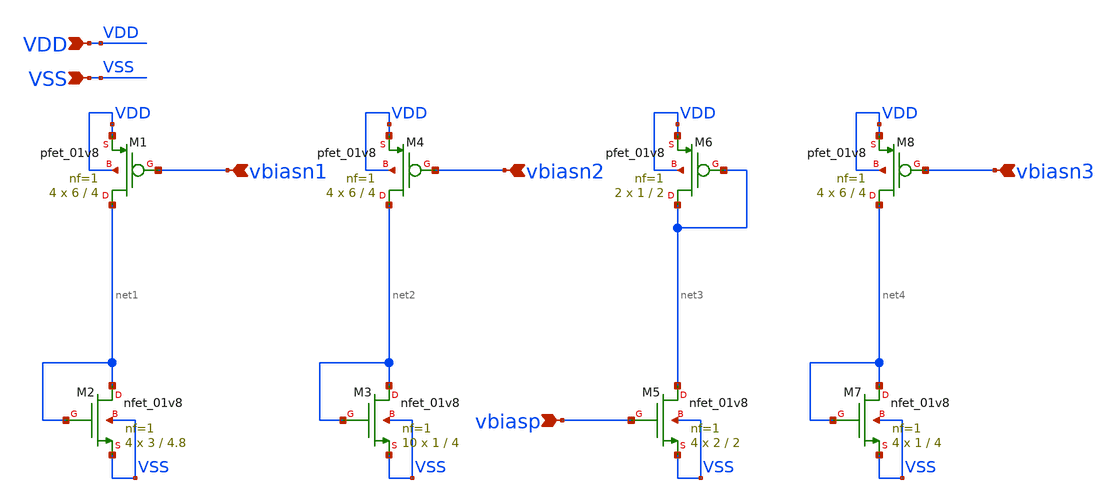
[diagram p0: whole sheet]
** sch_path: designs/bias_current_distribution.sch
* Copyright 2020 Stefan Frederik Schippers
* Licensed under the Apache License, Version 2.0 (the "License");
* you may not use this file except in compliance with the License.
* You may obtain a copy of the License at
* https://www.apache.org/licenses/LICENSE-2.0
* Unless required by applicable law or agreed to in writing, software
* distributed under the License is distributed on an "AS IS" BASIS,
* WITHOUT WARRANTIES OR CONDITIONS OF ANY KIND, either express or implied.
* See the License for the specific language governing permissions and
* limitations under the License.
**.subckt bias_current_distribution VDD VSS vbiasn1 vbiasn2 vbiasp vbiasn3
*.ipin VDD
*.ipin VSS
*.ipin vbiasn1
*.ipin vbiasn2
*.ipin vbiasp
*.ipin vbiasn3
XM2 net1 net1 VSS VSS sky130_fd_pr__nfet_01v8 L=4.8 W=3 nf=1 ad='int((nf+1)/2) * W/nf * 0.29' as='int((nf+2)/2) * W/nf * 0.29'
+ pd='2*int((nf+1)/2) * (W/nf + 0.29)' ps='2*int((nf+2)/2) * (W/nf + 0.29)' nrd='0.29 / W' nrs='0.29 / W'
+ sa=0 sb=0 sd=0 mult=4 m=4
XM1 net1 vbiasn1 VDD VDD sky130_fd_pr__pfet_01v8 L=4 W=6 nf=1 ad='int((nf+1)/2) * W/nf * 0.29' as='int((nf+2)/2) * W/nf * 0.29'
+ pd='2*int((nf+1)/2) * (W/nf + 0.29)' ps='2*int((nf+2)/2) * (W/nf + 0.29)' nrd='0.29 / W' nrs='0.29 / W'
+ sa=0 sb=0 sd=0 mult=4 m=4
XM3 net2 net2 VSS VSS sky130_fd_pr__nfet_01v8 L=4 W=1 nf=1 ad='int((nf+1)/2) * W/nf * 0.29' as='int((nf+2)/2) * W/nf * 0.29'
+ pd='2*int((nf+1)/2) * (W/nf + 0.29)' ps='2*int((nf+2)/2) * (W/nf + 0.29)' nrd='0.29 / W' nrs='0.29 / W'
+ sa=0 sb=0 sd=0 mult=10 m=10
XM4 net2 vbiasn2 VDD VDD sky130_fd_pr__pfet_01v8 L=4 W=6 nf=1 ad='int((nf+1)/2) * W/nf * 0.29' as='int((nf+2)/2) * W/nf * 0.29'
+ pd='2*int((nf+1)/2) * (W/nf + 0.29)' ps='2*int((nf+2)/2) * (W/nf + 0.29)' nrd='0.29 / W' nrs='0.29 / W'
+ sa=0 sb=0 sd=0 mult=4 m=4
XM5 net3 vbiasp VSS VSS sky130_fd_pr__nfet_01v8 L=2 W=2 nf=1 ad='int((nf+1)/2) * W/nf * 0.29' as='int((nf+2)/2) * W/nf * 0.29'
+ pd='2*int((nf+1)/2) * (W/nf + 0.29)' ps='2*int((nf+2)/2) * (W/nf + 0.29)' nrd='0.29 / W' nrs='0.29 / W'
+ sa=0 sb=0 sd=0 mult=4 m=4
XM6 net3 net3 VDD VDD sky130_fd_pr__pfet_01v8 L=2 W=1 nf=1 ad='int((nf+1)/2) * W/nf * 0.29' as='int((nf+2)/2) * W/nf * 0.29'
+ pd='2*int((nf+1)/2) * (W/nf + 0.29)' ps='2*int((nf+2)/2) * (W/nf + 0.29)' nrd='0.29 / W' nrs='0.29 / W'
+ sa=0 sb=0 sd=0 mult=2 m=2
XM7 net4 net4 VSS VSS sky130_fd_pr__nfet_01v8 L=4 W=1 nf=1 ad='int((nf+1)/2) * W/nf * 0.29' as='int((nf+2)/2) * W/nf * 0.29'
+ pd='2*int((nf+1)/2) * (W/nf + 0.29)' ps='2*int((nf+2)/2) * (W/nf + 0.29)' nrd='0.29 / W' nrs='0.29 / W'
+ sa=0 sb=0 sd=0 mult=4 m=4
XM8 net4 vbiasn3 VDD VDD sky130_fd_pr__pfet_01v8 L=4 W=6 nf=1 ad='int((nf+1)/2) * W/nf * 0.29' as='int((nf+2)/2) * W/nf * 0.29'
+ pd='2*int((nf+1)/2) * (W/nf + 0.29)' ps='2*int((nf+2)/2) * (W/nf + 0.29)' nrd='0.29 / W' nrs='0.29 / W'
+ sa=0 sb=0 sd=0 mult=4 m=4
**.ends
.end
